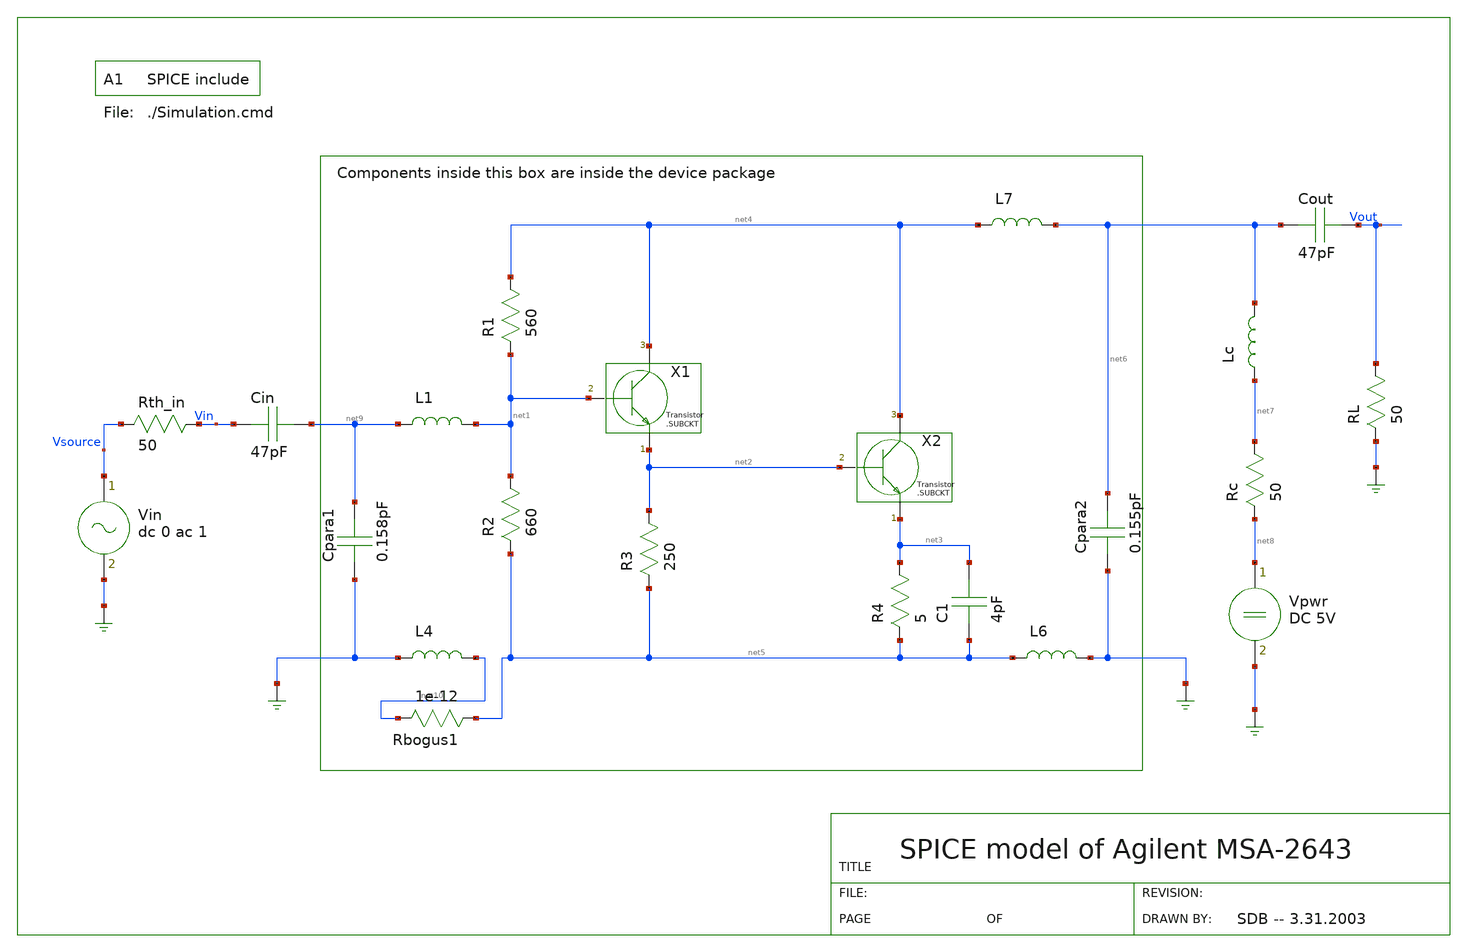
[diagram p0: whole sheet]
** sch_path: xschem_library/gschem_import/MSA-2643.sch
**.subckt MSA-2643
R1 net1 net4 560
R2 net5 net1 660
R3 net5 net2 250
R4 net5 net3 5
X1 net4 net1 net2
X2 net4 net2 net3
C1 net5 net3 4pF
Vpwr net8 GND DC 5V
Vin Vsource GND dc 0 ac 1
Rth_in Vsource Vin 50
RL GND Vout 50
Lc net7 net6 22nH
Rc net8 net7 50
Cout net6 Vout 47pF
Cin Vin net9 47pF
.include ./Simulation.cmd
L4 GND net10 0.386nH
L6 net5 GND 0.313nH
L1 net9 net1 0.833nH
L7 net4 net6 0.407nH
Cpara1 GND net9 0.158pF
Cpara2 GND net6 0.155pF
Rbogus1 net5 net10 1e-12
**.ends
.end
